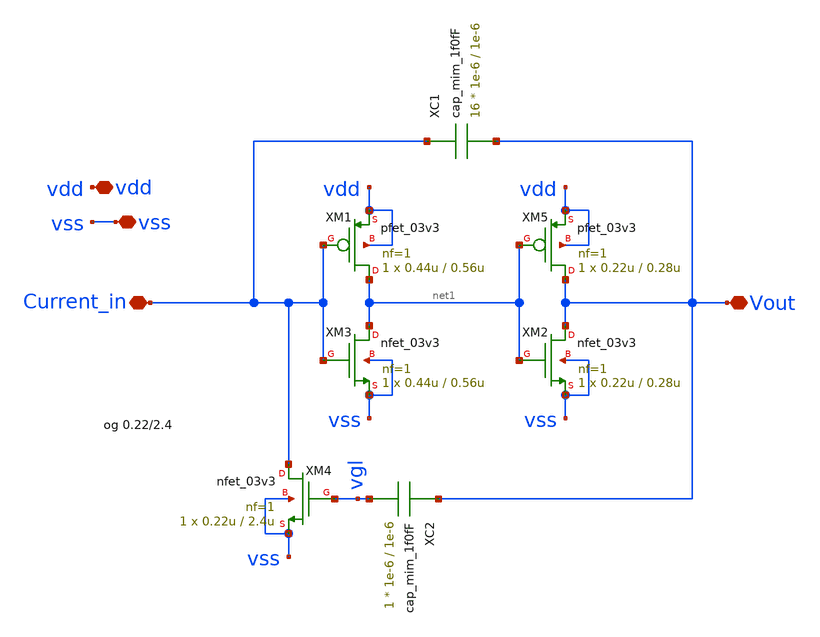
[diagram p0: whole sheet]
** sch_path: designs/libs/core_AH_neuron/AH_neuron.sch
**.subckt AH_neuron vdd vss Current_in Vout
*.iopin vdd
*.iopin vss
*.iopin Current_in
*.iopin Vout
XM5 Vout net1 vdd vdd pfet_03v3 L=0.28u W=0.22u nf=1 ad='int((nf+1)/2) * W/nf * 0.18u' as='int((nf+2)/2) * W/nf * 0.18u'
+ pd='2*int((nf+1)/2) * (W/nf + 0.18u)' ps='2*int((nf+2)/2) * (W/nf + 0.18u)' nrd='0.18u / W' nrs='0.18u / W'
+ sa=0 sb=0 sd=0 m=1
XM1 net1 Current_in vdd vdd pfet_03v3 L=0.56u W=0.44u nf=1 ad='int((nf+1)/2) * W/nf * 0.18u' as='int((nf+2)/2) * W/nf * 0.18u'
+ pd='2*int((nf+1)/2) * (W/nf + 0.18u)' ps='2*int((nf+2)/2) * (W/nf + 0.18u)' nrd='0.18u / W' nrs='0.18u / W'
+ sa=0 sb=0 sd=0 m=1
XM2 Vout net1 vss vss nfet_03v3 L=0.28u W=0.22u nf=1 ad='int((nf+1)/2) * W/nf * 0.18u' as='int((nf+2)/2) * W/nf * 0.18u'
+ pd='2*int((nf+1)/2) * (W/nf + 0.18u)' ps='2*int((nf+2)/2) * (W/nf + 0.18u)' nrd='0.18u / W' nrs='0.18u / W'
+ sa=0 sb=0 sd=0 m=1
XM3 net1 Current_in vss vss nfet_03v3 L=0.56u W=0.44u nf=1 ad='int((nf+1)/2) * W/nf * 0.18u' as='int((nf+2)/2) * W/nf * 0.18u'
+ pd='2*int((nf+1)/2) * (W/nf + 0.18u)' ps='2*int((nf+2)/2) * (W/nf + 0.18u)' nrd='0.18u / W' nrs='0.18u / W'
+ sa=0 sb=0 sd=0 m=1
XM4 Current_in vgl vss vss nfet_03v3 L=2.4u W=0.22u nf=1 ad='int((nf+1)/2) * W/nf * 0.18u' as='int((nf+2)/2) * W/nf * 0.18u'
+ pd='2*int((nf+1)/2) * (W/nf + 0.18u)' ps='2*int((nf+2)/2) * (W/nf + 0.18u)' nrd='0.18u / W' nrs='0.18u / W'
+ sa=0 sb=0 sd=0 m=1
XC1 Current_in Vout cap_mim_1f0fF c_width=1e-6 c_length=1e-6 m=16
XC2 Vout vgl cap_mim_1f0fF c_width=1e-6 c_length=1e-6 m=1
**.ends
.end
